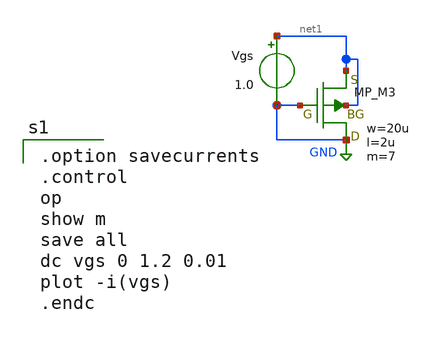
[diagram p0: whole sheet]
** sch_path: member_project/DCDC/ShuntaroOHNO/xschem/pmos_id_diode.sch
**.subckt pmos_id_diode
XM3 GND GND net1 net1 PMOS w=20u l=2u as=0 ad=0 ps=0 pd=0 nrd=0 nrs=0 m=7
Vgs net1 GND 1.0
**** begin user architecture code
 .include $::LIB/ip62_models

.option savecurrents
.control
op
show m
save all
dc vgs 0 1.2 0.01
plot -i(vgs)
.endc

**** end user architecture code
**.ends
.GLOBAL GND
.end
